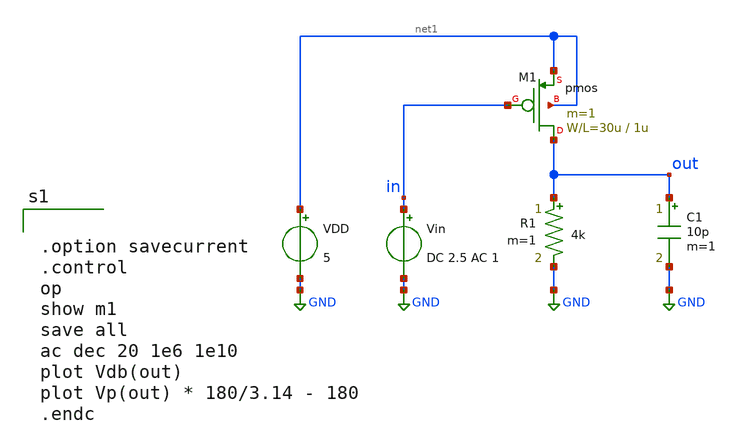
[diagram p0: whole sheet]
** sch_path: member_project/GroupWork/Team_masahiro/pfet_common_source_AC.sch
**.subckt pfet_common_source_AC
R1 out GND 4k m=1
VDD net1 GND 5
Vin in GND DC 2.5 AC 1
M1 out in net1 net1 pmos L=1u W=30u m=1
C1 out GND 10p m=1
**** begin user architecture code
 .include $::LIB/mos.lib
.include $::LIB/passive.lib
.include $::LIB/diode.lib


.option savecurrent
.control
op
show m1
save all
ac dec 20 1e6 1e10
plot Vdb(out)
plot Vp(out) * 180/3.14 - 180
.endc


**** end user architecture code
**.ends
.GLOBAL GND
.end
